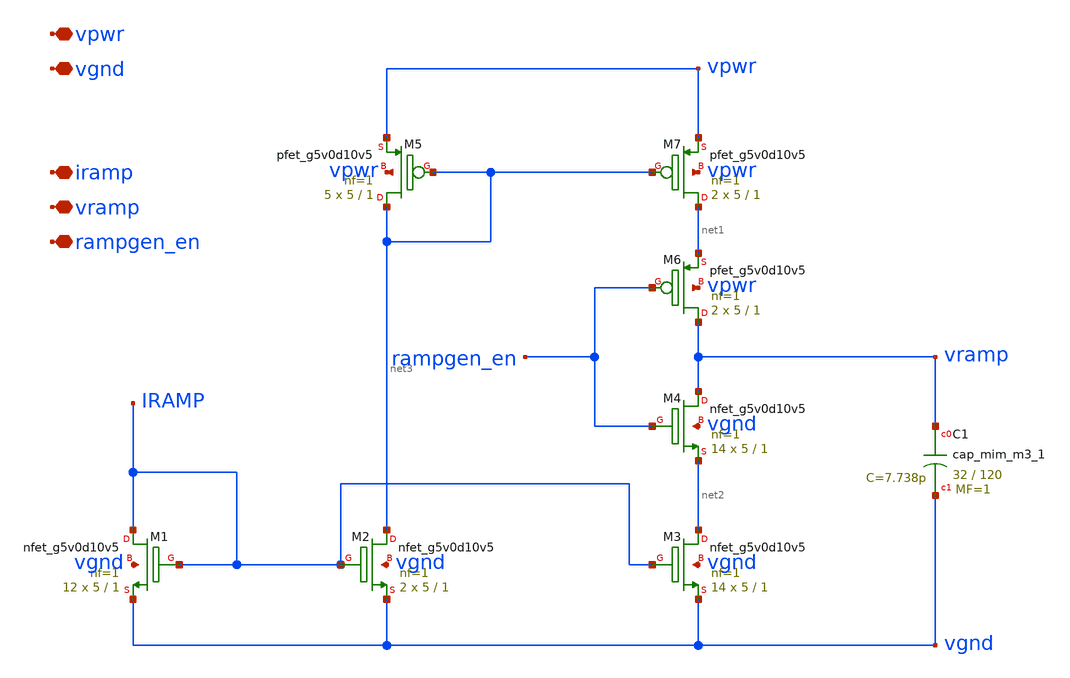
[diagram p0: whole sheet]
** sch_path: images/iic-osic-tools/addons/examples/open-pmic/design/oscillator/rampgen_wo_dummies.sch
**.subckt rampgen_wo_dummies vpwr vgnd iramp vramp rampgen_en
*.iopin vpwr
*.iopin vgnd
*.iopin iramp
*.iopin vramp
*.iopin rampgen_en
XM1 IRAMP IRAMP vgnd vgnd sky130_fd_pr__nfet_g5v0d10v5 L=1 W=5 nf=1 ad='int((nf+1)/2) * W/nf * 0.29'
+ as='int((nf+2)/2) * W/nf * 0.29' pd='2*int((nf+1)/2) * (W/nf + 0.29)' ps='2*int((nf+2)/2) * (W/nf + 0.29)'
+ nrd='0.29 / W' nrs='0.29 / W' sa=0 sb=0 sd=0 mult=12 m=12
XM2 net3 IRAMP vgnd vgnd sky130_fd_pr__nfet_g5v0d10v5 L=1 W=5 nf=1 ad='int((nf+1)/2) * W/nf * 0.29' as='int((nf+2)/2) * W/nf * 0.29'
+ pd='2*int((nf+1)/2) * (W/nf + 0.29)' ps='2*int((nf+2)/2) * (W/nf + 0.29)' nrd='0.29 / W' nrs='0.29 / W'
+ sa=0 sb=0 sd=0 mult=2 m=2
XM3 net2 IRAMP vgnd vgnd sky130_fd_pr__nfet_g5v0d10v5 L=1 W=5 nf=1 ad='int((nf+1)/2) * W/nf * 0.29' as='int((nf+2)/2) * W/nf * 0.29'
+ pd='2*int((nf+1)/2) * (W/nf + 0.29)' ps='2*int((nf+2)/2) * (W/nf + 0.29)' nrd='0.29 / W' nrs='0.29 / W'
+ sa=0 sb=0 sd=0 mult=14 m=14
XM4 vramp rampgen_en net2 vgnd sky130_fd_pr__nfet_g5v0d10v5 L=1 W=5 nf=1 ad='int((nf+1)/2) * W/nf * 0.29'
+ as='int((nf+2)/2) * W/nf * 0.29' pd='2*int((nf+1)/2) * (W/nf + 0.29)' ps='2*int((nf+2)/2) * (W/nf + 0.29)'
+ nrd='0.29 / W' nrs='0.29 / W' sa=0 sb=0 sd=0 mult=14 m=14
XM5 net3 net3 vpwr vpwr sky130_fd_pr__pfet_g5v0d10v5 L=1 W=5 nf=1 ad='int((nf+1)/2) * W/nf * 0.29' as='int((nf+2)/2) * W/nf * 0.29'
+ pd='2*int((nf+1)/2) * (W/nf + 0.29)' ps='2*int((nf+2)/2) * (W/nf + 0.29)' nrd='0.29 / W' nrs='0.29 / W'
+ sa=0 sb=0 sd=0 mult=5 m=5
XM6 vramp rampgen_en net1 vpwr sky130_fd_pr__pfet_g5v0d10v5 L=1 W=5 nf=1 ad='int((nf+1)/2) * W/nf * 0.29'
+ as='int((nf+2)/2) * W/nf * 0.29' pd='2*int((nf+1)/2) * (W/nf + 0.29)' ps='2*int((nf+2)/2) * (W/nf + 0.29)'
+ nrd='0.29 / W' nrs='0.29 / W' sa=0 sb=0 sd=0 mult=2 m=2
XM7 net1 net3 vpwr vpwr sky130_fd_pr__pfet_g5v0d10v5 L=1 W=5 nf=1 ad='int((nf+1)/2) * W/nf * 0.29' as='int((nf+2)/2) * W/nf * 0.29'
+ pd='2*int((nf+1)/2) * (W/nf + 0.29)' ps='2*int((nf+2)/2) * (W/nf + 0.29)' nrd='0.29 / W' nrs='0.29 / W'
+ sa=0 sb=0 sd=0 mult=2 m=2
XC1 vramp vgnd sky130_fd_pr__cap_mim_m3_1 W=32 L=120 MF=1 m=1
**.ends
.end
